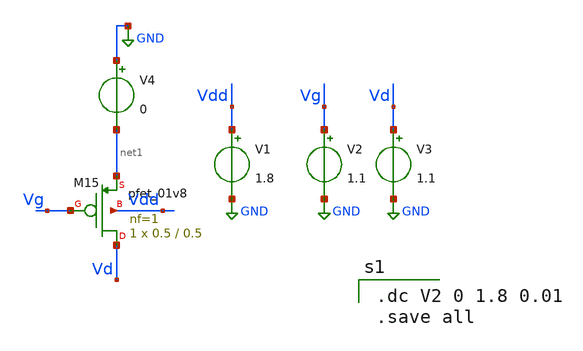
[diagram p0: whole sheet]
** sch_path: xschem/xschemfiles/ptest.sch
**.subckt ptest
XM15 Vd Vg net1 Vdd sky130_fd_pr__pfet_01v8 L=0.5 W=0.5 nf=1 ad='int((nf+1)/2) * W/nf * 0.29' as='int((nf+2)/2) * W/nf * 0.29'
+ pd='2*int((nf+1)/2) * (W/nf + 0.29)' ps='2*int((nf+2)/2) * (W/nf + 0.29)' nrd='0.29 / W' nrs='0.29 / W'
+ sa=0 sb=0 sd=0 mult=1 m=1
V1 Vdd GND 1.8
V2 Vg GND 1.1
V3 Vd GND 1.1
V4 GND net1 0
**** begin user architecture code

.dc V2 0 1.8 0.01
.save all


** opencircuitdesign pdks install
.lib $::SKYWATER_MODELS/sky130.lib.spice tt


**** end user architecture code
**.ends
.GLOBAL GND
.end
